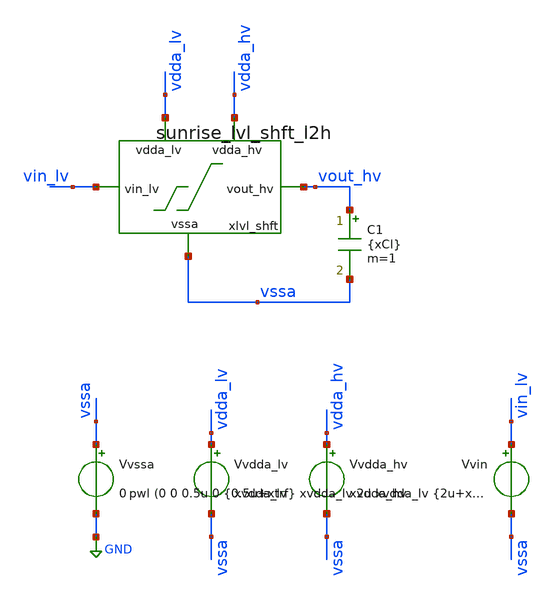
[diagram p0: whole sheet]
** sch_path: Design_Review_3/LVL_SHFT/tb_sunrise_lvl_shft.sch
**.subckt tb_sunrise_lvl_shft
Vvssa vssa GND 0
Vvdda_hv vdda_hv vssa xvdda_hv
Vvdda_lv vdda_lv vssa xvdda_lv
Vvin vin_lv vssa pwl (0 0 0.5u 0 {0.5u+xtrf} xvdda_lv 2u xvdda_lv {2u+xtrf} 0 3.5u 0 {3.5u+xtrf} xvdda_lv)
C1 vout_hv vssa {xCl} m=1
xlvl_shft vdda_hv vout_hv vdda_lv vin_lv vssa sunrise_lvl_shft_l2h
**** begin user architecture code

** opencircuitdesign pdks install
.lib /home/slice/pdk/iHP/IHP-Open-PDK/ihp-sg13g2/libs.tech/ngspice/models/cornerMOSlv.lib mos_tt
.lib /home/slice/pdk/iHP/IHP-Open-PDK/ihp-sg13g2/libs.tech/ngspice/models/cornerMOShv.lib mos_tt
.lib /home/slice/pdk/iHP/IHP-Open-PDK/ihp-sg13g2/libs.tech/ngspice/models/cornerRES.lib res_typ
*.lib /home/slice/pdk/iHP/IHP-Open-PDK/ihp-sg13g2/libs.tech/ngspice/models/cornerCAP.lib cap_typ
* SG13G2 STD CELLS
*.include /home/slice/pdk/iHP/IHP-Open-PDK/ihp-sg13g2/libs.ref/sg13g2_stdcell/spice/sg13g2_stdcell.spice
* SG13CMOS5L STD CELLS
.include /home/slice/pdk/iHP/IHP-Open-PDK/ihp-sg13cmos5l/libs.ref/sg13cmos5l_stdcell/spice/sg13cmos5l_stdcell.spice

* only to be used in extreme circumstances when circuit is not converging!
*.option rshunt=1e22

* Parameters
.param xvdda_hv = 3.3
.csparam xvdda_hv_var = 'xvdda_hv'
.param xvdda_lv = 1.5
.csparam xvdda_lv_var = 'xvdda_lv'
.param cor_id = 0
.csparam cor_id_var = 'cor_id'
.param xtsim = 5u
.csparam xtsim_var = 'xtsim'
.param xtstep = 1n
.csparam xtstep_var = 'xtstep'
.param xtrf = 100p
.param xCl = 0.1p

.temp 27

.include tb_sunrise_lvl_shft.save

.save all

.control

set xTj = ( 125 )
let xTj_var  = $xTj
set temp = $xTj

** 1. DCOP ANALYSIS **

  op
  remzerovec
  set filetype=binary
  ** first write deletes existing file
  write tb_sunrise_lvl_shft_dcop.raw

** 2. TRAN ANALYSIS **

  *set appendwrite
  tran $&xtstep_var $&xtsim_var
  *** always put remzerovec after the analysis statement!!!
  remzerovec
  write tb_sunrise_lvl_shft_tran.raw
 *unset appendwrite

 ** 3. TRAN MEASURES **

  echo --
  meas tran vin_lv_lo_1 AVG v(vin_lv) from=100n to=0.49u
  meas tran vout_hv_lo_1 AVG v(vout_hv) from=100n to=0.49u
  meas tran vin_lv_hi_1 AVG v(vin_lv) from=0.51u to=1.99u
  meas tran vout_hv_hi_1 AVG v(vout_hv) from=0.51u to=1.99u
  meas tran vin_lv_lo_2 AVG v(vin_lv) from=2.01u to=3.5u
  meas tran vout_hv_lo_2 AVG v(vout_hv) from=2.01u to=3.5u
  meas tran vin_lv_hi_2 AVG v(vin_lv) from=3.51u to=5u
  meas tran vout_hv_hi_2 AVG v(vout_hv) from=3.51u to=5u
  meas tran iddahv_max MAX i(vvdda_hv) from=100n to=$&xtsim_var
  let iddahv_max_mA = iddahv_max*(-1e3)

  * 3.0 Global parameters:
  echo cor_id = "$&cor_id_var"
  echo "$&cor_id_var" > vin_lv_hi.txt
  echo "$&cor_id_var" > vin_lv_lo.txt
  echo "$&cor_id_var" > vout_hv_hi.txt
  echo "$&cor_id_var" > vout_hv_lo.txt
  echo --
  echo temp = "$temp"
  echo "$temp" >> vin_lv_hi.txt
  echo "$temp" >> vin_lv_lo.txt
  echo "$temp" >> vout_hv_hi.txt
  echo "$temp" >> vout_hv_lo.txt
  echo --
  echo vdda_hv = "$&xvdda_hv_var"
  echo "$&xvdda_hv_var" >> vin_lv_hi.txt
  echo "$&xvdda_hv_var" >> vin_lv_lo.txt
  echo "$&xvdda_hv_var" >> vout_hv_hi.txt
  echo "$&xvdda_hv_var" >> vout_hv_lo.txt
  echo --
  echo vdda_lv = "$&xvdda_lv_var"
  echo "$&xvdda_lv_var" >> vin_lv_hi.txt
  echo "$&xvdda_lv_var" >> vin_lv_lo.txt
  echo "$&xvdda_lv_var" >> vout_hv_hi.txt
  echo "$&xvdda_lv_var" >> vout_hv_lo.txt
  echo --
  echo "$&vin_lv_lo_1" >> vin_lv_lo.txt
  echo "$&vin_lv_lo_2" >> vin_lv_lo.txt
  echo "$&vin_lv_hi_1" >> vin_lv_hi.txt
  echo "$&vin_lv_hi_2" >> vin_lv_hi.txt
  echo "$&vout_hv_lo_1" >> vout_hv_lo.txt
  echo "$&vout_hv_lo_2" >> vout_hv_lo.txt
  echo "$&vout_hv_hi_1" >> vout_hv_hi.txt
  echo "$&vout_hv_hi_2" >> vout_hv_hi.txt

  echo --

  setplot
quit 0
.endc




**** end user architecture code
**.ends

* expanding   symbol:  sunrise/sunrise_lvl_shft_l2h.sym # of pins=5
** sym_path: Schematics_Layout/sunrise_lvl_shft_l2h/sunrise_lvl_shft_l2h.sym
** sch_path: Schematics_Layout/sunrise_lvl_shft_l2h/sunrise_lvl_shft_l2h.sch
.subckt sunrise_lvl_shft_l2h vdda_hv vout_hv vdda_lv vin_lv vssa
*.ipin vdda_hv
*.ipin vdda_lv
*.ipin vssa
*.ipin vin_lv
*.opin vout_hv
XM1 lvlsh in_b vssa vssa sg13_hv_nmos w=2u l=0.45u ng=1 m=1 mm_ok=1
XM2 lvlsh_b vin_lv vssa vssa sg13_hv_nmos w=2u l=0.45u ng=1 m=1 mm_ok=1
XM3 lvlsh lvlsh_b vdda_hv vdda_hv sg13_hv_pmos w=0.3u l=0.45u ng=1 m=1 mm_ok=1
XM4 lvlsh_b lvlsh vdda_hv vdda_hv sg13_hv_pmos w=0.3u l=0.45u ng=1 m=1 mm_ok=1
XM7 vout_hv lvlsh_b vssa vssa sg13_hv_nmos w=2u l=0.45u ng=1 m=1 mm_ok=1
XM8 vout_hv lvlsh_b vdda_hv vdda_hv sg13_hv_pmos w=2u l=0.4u ng=1 m=2 mm_ok=1
x1 in_b vin_lv vdda_lv vssa sg13cmos5l_inv_2
* noconn vdda_lv
.ends

.GLOBAL GND
.end
